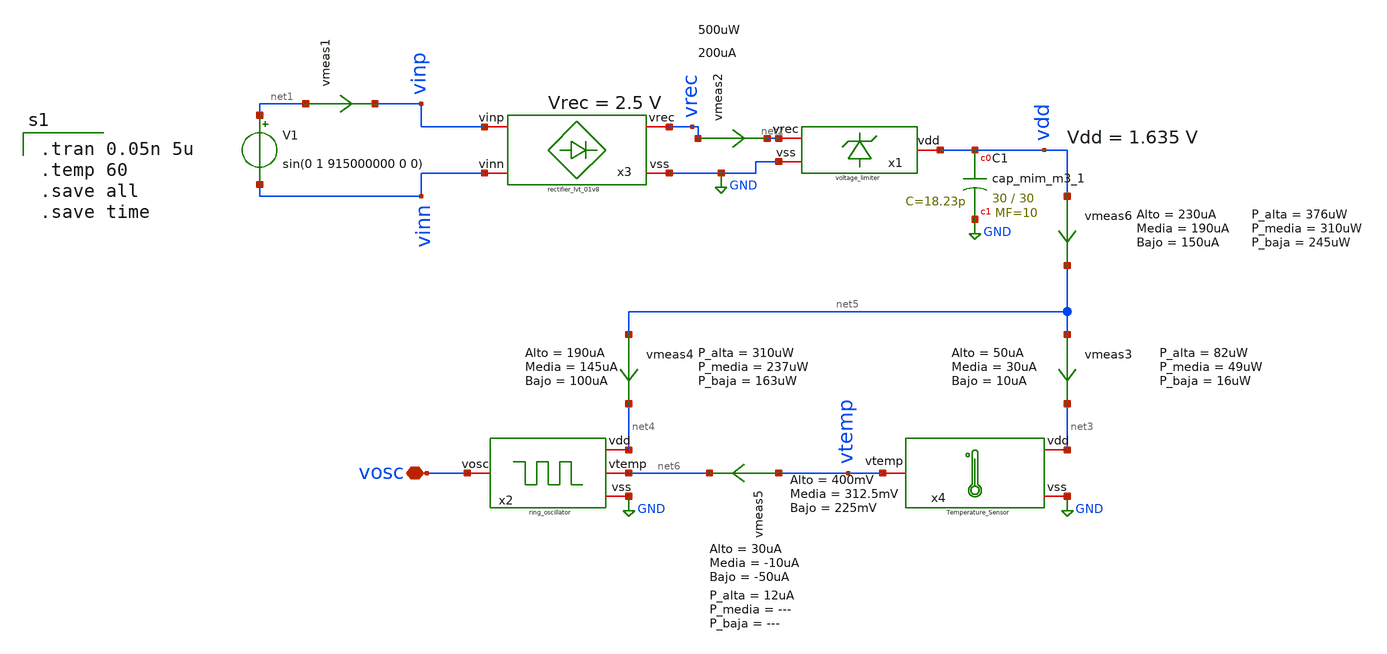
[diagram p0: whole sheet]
** sch_path: XSCHEM/system_on_chip_with_lim.sch
**.subckt system_on_chip_with_lim vosc
*.iopin vosc
V1 net1 vinn sin(0 1 915000000 0 0)
vmeas2 vrec net2 0
.save i(vmeas2)
vmeas1 net1 vinp 0
.save i(vmeas1)
XC1 vdd GND sky130_fd_pr__cap_mim_m3_1 W=30 L=30 MF=10 m=10
x2 net4 vosc GND net6 ring_oscillator
x3 vinp vrec vinn GND rectifier_lvt_01v8
x4 net3 vtemp GND Temperature_Sensor
vmeas3 net5 net3 0
.save i(vmeas3)
vmeas4 net5 net4 0
.save i(vmeas4)
vmeas5 vtemp net6 0
.save i(vmeas5)
x1 net2 vdd GND voltage_limiter
vmeas6 vdd net5 0
.save i(vmeas6)
**** begin user architecture code

.tran 0.05n 5u
.temp 60
.save all
.save time


** opencircuitdesign pdks install
.lib $::SKYWATER_MODELS/sky130.lib.spice tt


**** end user architecture code
**.ends

* expanding   symbol:  Documentos/TESIS DE
*+ GRADO/WORK_IN_PROGRESS/My_xschem_prueba/ring_oscillator.sym # of pins=4
** sym_path: XSCHEM/ring_oscillator.sym
** sch_path: XSCHEM/ring_oscillator.sch
.subckt ring_oscillator vdd vosc vss vtemp
*.iopin vtemp
*.iopin vss
*.iopin vdd
*.iopin vosc
XM7 net1 vosc vdd vdd sky130_fd_pr__pfet_01v8_lvt L=2 W=12 nf=1 ad='int((nf+1)/2) * W/nf * 0.29' as='int((nf+2)/2) * W/nf * 0.29'
+ pd='2*int((nf+1)/2) * (W/nf + 0.29)' ps='2*int((nf+2)/2) * (W/nf + 0.29)' nrd='0.29 / W' nrs='0.29 / W'
+ sa=0 sb=0 sd=0 mult=1 m=1
XM8 net1 vosc vss vss sky130_fd_pr__nfet_01v8_lvt L=2 W=4 nf=1 ad='int((nf+1)/2) * W/nf * 0.29' as='int((nf+2)/2) * W/nf * 0.29'
+ pd='2*int((nf+1)/2) * (W/nf + 0.29)' ps='2*int((nf+2)/2) * (W/nf + 0.29)' nrd='0.29 / W' nrs='0.29 / W'
+ sa=0 sb=0 sd=0 mult=1 m=1
XM9 net2 net1 vdd vdd sky130_fd_pr__pfet_01v8_lvt L=2 W=12 nf=1 ad='int((nf+1)/2) * W/nf * 0.29' as='int((nf+2)/2) * W/nf * 0.29'
+ pd='2*int((nf+1)/2) * (W/nf + 0.29)' ps='2*int((nf+2)/2) * (W/nf + 0.29)' nrd='0.29 / W' nrs='0.29 / W'
+ sa=0 sb=0 sd=0 mult=1 m=1
XM10 net2 net1 vss vss sky130_fd_pr__nfet_01v8_lvt L=2 W=4 nf=1 ad='int((nf+1)/2) * W/nf * 0.29' as='int((nf+2)/2) * W/nf * 0.29'
+ pd='2*int((nf+1)/2) * (W/nf + 0.29)' ps='2*int((nf+2)/2) * (W/nf + 0.29)' nrd='0.29 / W' nrs='0.29 / W'
+ sa=0 sb=0 sd=0 mult=1 m=1
XM11 vosc net2 vdd vdd sky130_fd_pr__pfet_01v8_lvt L=2 W=12 nf=1 ad='int((nf+1)/2) * W/nf * 0.29' as='int((nf+2)/2) * W/nf * 0.29'
+ pd='2*int((nf+1)/2) * (W/nf + 0.29)' ps='2*int((nf+2)/2) * (W/nf + 0.29)' nrd='0.29 / W' nrs='0.29 / W'
+ sa=0 sb=0 sd=0 mult=1 m=1
XM12 vosc net2 vss vss sky130_fd_pr__nfet_01v8_lvt L=2 W=4 nf=1 ad='int((nf+1)/2) * W/nf * 0.29' as='int((nf+2)/2) * W/nf * 0.29'
+ pd='2*int((nf+1)/2) * (W/nf + 0.29)' ps='2*int((nf+2)/2) * (W/nf + 0.29)' nrd='0.29 / W' nrs='0.29 / W'
+ sa=0 sb=0 sd=0 mult=1 m=1
XC1 vosc vtemp vss sky130_fd_pr__cap_var_lvt W=5 L=5 VM=1 m=1
XC2 net2 vtemp vss sky130_fd_pr__cap_var_lvt W=5 L=5 VM=1 m=1
XC3 net1 vtemp vss sky130_fd_pr__cap_var_lvt W=5 L=5 VM=1 m=1
.ends


* expanding   symbol:  Documentos/TESIS DE
*+ GRADO/WORK_IN_PROGRESS/My_xschem_prueba/rectifier_lvt_01v8.sym # of pins=4
** sym_path: XSCHEM/rectifier_lvt_01v8.sym
** sch_path: XSCHEM/rectifier_lvt_01v8.sch
.subckt rectifier_lvt_01v8 vinp vrec vinn vss
*.iopin vinp
*.iopin vinn
*.iopin vss
*.iopin vrec
XC11 vinp net3 sky130_fd_pr__cap_mim_m3_1 W=30 L=30 MF=1 m=1
XC12 net2 vinn sky130_fd_pr__cap_mim_m3_1 W=30 L=30 MF=1 m=1
XC13 vinp net6 sky130_fd_pr__cap_mim_m3_1 W=30 L=30 MF=1 m=1
XC14 net5 vinn sky130_fd_pr__cap_mim_m3_1 W=30 L=30 MF=1 m=1
XM25 vinp vinn vss vss sky130_fd_pr__nfet_01v8_lvt L=0.18 W=5 nf=1 ad='int((nf+1)/2) * W/nf * 0.29' as='int((nf+2)/2) * W/nf * 0.29'
+ pd='2*int((nf+1)/2) * (W/nf + 0.29)' ps='2*int((nf+2)/2) * (W/nf + 0.29)' nrd='0.29 / W' nrs='0.29 / W'
+ sa=0 sb=0 sd=0 mult=6 m=6
XM26 vinn vinp vss vss sky130_fd_pr__nfet_01v8_lvt L=0.18 W=5 nf=1 ad='int((nf+1)/2) * W/nf * 0.29' as='int((nf+2)/2) * W/nf * 0.29'
+ pd='2*int((nf+1)/2) * (W/nf + 0.29)' ps='2*int((nf+2)/2) * (W/nf + 0.29)' nrd='0.29 / W' nrs='0.29 / W'
+ sa=0 sb=0 sd=0 mult=6 m=6
XM27 vinp vinn net1 net1 sky130_fd_pr__pfet_01v8_lvt L=0.35 W=10 nf=2 ad='int((nf+1)/2) * W/nf * 0.29'
+ as='int((nf+2)/2) * W/nf * 0.29' pd='2*int((nf+1)/2) * (W/nf + 0.29)' ps='2*int((nf+2)/2) * (W/nf + 0.29)'
+ nrd='0.29 / W' nrs='0.29 / W' sa=0 sb=0 sd=0 mult=3 m=3
XM28 vinn vinp net1 net1 sky130_fd_pr__pfet_01v8_lvt L=0.35 W=10 nf=2 ad='int((nf+1)/2) * W/nf * 0.29'
+ as='int((nf+2)/2) * W/nf * 0.29' pd='2*int((nf+1)/2) * (W/nf + 0.29)' ps='2*int((nf+2)/2) * (W/nf + 0.29)'
+ nrd='0.29 / W' nrs='0.29 / W' sa=0 sb=0 sd=0 mult=3 m=3
XM29 net3 net2 net1 vss sky130_fd_pr__nfet_01v8_lvt L=0.18 W=5 nf=1 ad='int((nf+1)/2) * W/nf * 0.29'
+ as='int((nf+2)/2) * W/nf * 0.29' pd='2*int((nf+1)/2) * (W/nf + 0.29)' ps='2*int((nf+2)/2) * (W/nf + 0.29)'
+ nrd='0.29 / W' nrs='0.29 / W' sa=0 sb=0 sd=0 mult=6 m=6
XM30 net2 net3 net1 vss sky130_fd_pr__nfet_01v8_lvt L=0.18 W=5 nf=1 ad='int((nf+1)/2) * W/nf * 0.29'
+ as='int((nf+2)/2) * W/nf * 0.29' pd='2*int((nf+1)/2) * (W/nf + 0.29)' ps='2*int((nf+2)/2) * (W/nf + 0.29)'
+ nrd='0.29 / W' nrs='0.29 / W' sa=0 sb=0 sd=0 mult=6 m=6
XM31 net3 net2 net4 net4 sky130_fd_pr__pfet_01v8_lvt L=0.35 W=10 nf=2 ad='int((nf+1)/2) * W/nf * 0.29'
+ as='int((nf+2)/2) * W/nf * 0.29' pd='2*int((nf+1)/2) * (W/nf + 0.29)' ps='2*int((nf+2)/2) * (W/nf + 0.29)'
+ nrd='0.29 / W' nrs='0.29 / W' sa=0 sb=0 sd=0 mult=3 m=3
XM32 net2 net3 net4 net4 sky130_fd_pr__pfet_01v8_lvt L=0.35 W=10 nf=2 ad='int((nf+1)/2) * W/nf * 0.29'
+ as='int((nf+2)/2) * W/nf * 0.29' pd='2*int((nf+1)/2) * (W/nf + 0.29)' ps='2*int((nf+2)/2) * (W/nf + 0.29)'
+ nrd='0.29 / W' nrs='0.29 / W' sa=0 sb=0 sd=0 mult=3 m=3
XM33 net6 net5 net4 vss sky130_fd_pr__nfet_01v8_lvt L=0.18 W=5 nf=1 ad='int((nf+1)/2) * W/nf * 0.29'
+ as='int((nf+2)/2) * W/nf * 0.29' pd='2*int((nf+1)/2) * (W/nf + 0.29)' ps='2*int((nf+2)/2) * (W/nf + 0.29)'
+ nrd='0.29 / W' nrs='0.29 / W' sa=0 sb=0 sd=0 mult=6 m=6
XM34 net5 net6 net4 vss sky130_fd_pr__nfet_01v8_lvt L=0.18 W=5 nf=1 ad='int((nf+1)/2) * W/nf * 0.29'
+ as='int((nf+2)/2) * W/nf * 0.29' pd='2*int((nf+1)/2) * (W/nf + 0.29)' ps='2*int((nf+2)/2) * (W/nf + 0.29)'
+ nrd='0.29 / W' nrs='0.29 / W' sa=0 sb=0 sd=0 mult=6 m=6
XM35 net6 net5 net7 net7 sky130_fd_pr__pfet_01v8_lvt L=0.35 W=10 nf=2 ad='int((nf+1)/2) * W/nf * 0.29'
+ as='int((nf+2)/2) * W/nf * 0.29' pd='2*int((nf+1)/2) * (W/nf + 0.29)' ps='2*int((nf+2)/2) * (W/nf + 0.29)'
+ nrd='0.29 / W' nrs='0.29 / W' sa=0 sb=0 sd=0 mult=3 m=3
XM36 net5 net6 net7 net7 sky130_fd_pr__pfet_01v8_lvt L=0.35 W=10 nf=2 ad='int((nf+1)/2) * W/nf * 0.29'
+ as='int((nf+2)/2) * W/nf * 0.29' pd='2*int((nf+1)/2) * (W/nf + 0.29)' ps='2*int((nf+2)/2) * (W/nf + 0.29)'
+ nrd='0.29 / W' nrs='0.29 / W' sa=0 sb=0 sd=0 mult=3 m=3
XC15 vinp net9 sky130_fd_pr__cap_mim_m3_1 W=30 L=30 MF=1 m=1
XC16 net8 vinn sky130_fd_pr__cap_mim_m3_1 W=30 L=30 MF=1 m=1
XM37 net9 net8 net7 vss sky130_fd_pr__nfet_01v8_lvt L=0.18 W=5 nf=1 ad='int((nf+1)/2) * W/nf * 0.29'
+ as='int((nf+2)/2) * W/nf * 0.29' pd='2*int((nf+1)/2) * (W/nf + 0.29)' ps='2*int((nf+2)/2) * (W/nf + 0.29)'
+ nrd='0.29 / W' nrs='0.29 / W' sa=0 sb=0 sd=0 mult=6 m=6
XM38 net8 net9 net7 vss sky130_fd_pr__nfet_01v8_lvt L=0.18 W=5 nf=1 ad='int((nf+1)/2) * W/nf * 0.29'
+ as='int((nf+2)/2) * W/nf * 0.29' pd='2*int((nf+1)/2) * (W/nf + 0.29)' ps='2*int((nf+2)/2) * (W/nf + 0.29)'
+ nrd='0.29 / W' nrs='0.29 / W' sa=0 sb=0 sd=0 mult=6 m=6
XM39 net9 net8 net10 net10 sky130_fd_pr__pfet_01v8_lvt L=0.35 W=10 nf=2 ad='int((nf+1)/2) * W/nf * 0.29'
+ as='int((nf+2)/2) * W/nf * 0.29' pd='2*int((nf+1)/2) * (W/nf + 0.29)' ps='2*int((nf+2)/2) * (W/nf + 0.29)'
+ nrd='0.29 / W' nrs='0.29 / W' sa=0 sb=0 sd=0 mult=3 m=3
XM40 net8 net9 net10 net10 sky130_fd_pr__pfet_01v8_lvt L=0.35 W=10 nf=2 ad='int((nf+1)/2) * W/nf * 0.29'
+ as='int((nf+2)/2) * W/nf * 0.29' pd='2*int((nf+1)/2) * (W/nf + 0.29)' ps='2*int((nf+2)/2) * (W/nf + 0.29)'
+ nrd='0.29 / W' nrs='0.29 / W' sa=0 sb=0 sd=0 mult=3 m=3
XC17 vinp net12 sky130_fd_pr__cap_mim_m3_1 W=30 L=30 MF=1 m=1
XC18 net11 vinn sky130_fd_pr__cap_mim_m3_1 W=30 L=30 MF=1 m=1
XM41 net12 net11 net10 vss sky130_fd_pr__nfet_01v8_lvt L=0.18 W=5 nf=1 ad='int((nf+1)/2) * W/nf * 0.29'
+ as='int((nf+2)/2) * W/nf * 0.29' pd='2*int((nf+1)/2) * (W/nf + 0.29)' ps='2*int((nf+2)/2) * (W/nf + 0.29)'
+ nrd='0.29 / W' nrs='0.29 / W' sa=0 sb=0 sd=0 mult=6 m=6
XM42 net11 net12 net10 vss sky130_fd_pr__nfet_01v8_lvt L=0.18 W=5 nf=1 ad='int((nf+1)/2) * W/nf * 0.29'
+ as='int((nf+2)/2) * W/nf * 0.29' pd='2*int((nf+1)/2) * (W/nf + 0.29)' ps='2*int((nf+2)/2) * (W/nf + 0.29)'
+ nrd='0.29 / W' nrs='0.29 / W' sa=0 sb=0 sd=0 mult=6 m=6
XM43 net12 net11 net13 net13 sky130_fd_pr__pfet_01v8_lvt L=0.35 W=10 nf=2 ad='int((nf+1)/2) * W/nf * 0.29'
+ as='int((nf+2)/2) * W/nf * 0.29' pd='2*int((nf+1)/2) * (W/nf + 0.29)' ps='2*int((nf+2)/2) * (W/nf + 0.29)'
+ nrd='0.29 / W' nrs='0.29 / W' sa=0 sb=0 sd=0 mult=3 m=3
XM44 net11 net12 net13 net13 sky130_fd_pr__pfet_01v8_lvt L=0.35 W=10 nf=2 ad='int((nf+1)/2) * W/nf * 0.29'
+ as='int((nf+2)/2) * W/nf * 0.29' pd='2*int((nf+1)/2) * (W/nf + 0.29)' ps='2*int((nf+2)/2) * (W/nf + 0.29)'
+ nrd='0.29 / W' nrs='0.29 / W' sa=0 sb=0 sd=0 mult=3 m=3
XC19 vrec vss sky130_fd_pr__cap_mim_m3_1 W=30 L=30 MF=2 m=2
XC20 vinp net15 sky130_fd_pr__cap_mim_m3_1 W=30 L=30 MF=1 m=1
XC21 net14 vinn sky130_fd_pr__cap_mim_m3_1 W=30 L=30 MF=1 m=1
XM45 net15 net14 net13 vss sky130_fd_pr__nfet_01v8_lvt L=0.18 W=5 nf=1 ad='int((nf+1)/2) * W/nf * 0.29'
+ as='int((nf+2)/2) * W/nf * 0.29' pd='2*int((nf+1)/2) * (W/nf + 0.29)' ps='2*int((nf+2)/2) * (W/nf + 0.29)'
+ nrd='0.29 / W' nrs='0.29 / W' sa=0 sb=0 sd=0 mult=6 m=6
XM46 net14 net15 net13 vss sky130_fd_pr__nfet_01v8_lvt L=0.18 W=5 nf=1 ad='int((nf+1)/2) * W/nf * 0.29'
+ as='int((nf+2)/2) * W/nf * 0.29' pd='2*int((nf+1)/2) * (W/nf + 0.29)' ps='2*int((nf+2)/2) * (W/nf + 0.29)'
+ nrd='0.29 / W' nrs='0.29 / W' sa=0 sb=0 sd=0 mult=6 m=6
XM47 net15 net14 vrec vrec sky130_fd_pr__pfet_01v8_lvt L=0.35 W=10 nf=2 ad='int((nf+1)/2) * W/nf * 0.29'
+ as='int((nf+2)/2) * W/nf * 0.29' pd='2*int((nf+1)/2) * (W/nf + 0.29)' ps='2*int((nf+2)/2) * (W/nf + 0.29)'
+ nrd='0.29 / W' nrs='0.29 / W' sa=0 sb=0 sd=0 mult=3 m=3
XM48 net14 net15 vrec vrec sky130_fd_pr__pfet_01v8_lvt L=0.35 W=10 nf=2 ad='int((nf+1)/2) * W/nf * 0.29'
+ as='int((nf+2)/2) * W/nf * 0.29' pd='2*int((nf+1)/2) * (W/nf + 0.29)' ps='2*int((nf+2)/2) * (W/nf + 0.29)'
+ nrd='0.29 / W' nrs='0.29 / W' sa=0 sb=0 sd=0 mult=3 m=3
.ends


* expanding   symbol:  Documentos/TESIS DE
*+ GRADO/WORK_IN_PROGRESS/My_xschem_prueba/Temperature_Sensor.sym # of pins=3
** sym_path: XSCHEM/Temperature_Sensor.sym
** sch_path: XSCHEM/Temperature_Sensor.sch
.subckt Temperature_Sensor vdd vtemp vss
*.iopin vdd
*.iopin vss
*.iopin vtemp
XM8 net1 net4 net2 vss sky130_fd_pr__nfet_01v8_lvt L=2 W=1 nf=1 ad='int((nf+1)/2) * W/nf * 0.29' as='int((nf+2)/2) * W/nf * 0.29'
+ pd='2*int((nf+1)/2) * (W/nf + 0.29)' ps='2*int((nf+2)/2) * (W/nf + 0.29)' nrd='0.29 / W' nrs='0.29 / W'
+ sa=0 sb=0 sd=0 mult=4 m=4
XM9 vtemp net3 net2 vss sky130_fd_pr__nfet_01v8_lvt L=0.5 W=1 nf=1 ad='int((nf+1)/2) * W/nf * 0.29' as='int((nf+2)/2) * W/nf * 0.29'
+ pd='2*int((nf+1)/2) * (W/nf + 0.29)' ps='2*int((nf+2)/2) * (W/nf + 0.29)' nrd='0.29 / W' nrs='0.29 / W'
+ sa=0 sb=0 sd=0 mult=4 m=4
XM10 net2 net5 vss vss sky130_fd_pr__nfet_01v8 L=2 W=5 nf=1 ad='int((nf+1)/2) * W/nf * 0.29' as='int((nf+2)/2) * W/nf * 0.29'
+ pd='2*int((nf+1)/2) * (W/nf + 0.29)' ps='2*int((nf+2)/2) * (W/nf + 0.29)' nrd='0.29 / W' nrs='0.29 / W'
+ sa=0 sb=0 sd=0 mult=4 m=4
XM11 net1 net1 vdd vdd sky130_fd_pr__pfet_01v8_lvt L=2 W=5 nf=1 ad='int((nf+1)/2) * W/nf * 0.29' as='int((nf+2)/2) * W/nf * 0.29'
+ pd='2*int((nf+1)/2) * (W/nf + 0.29)' ps='2*int((nf+2)/2) * (W/nf + 0.29)' nrd='0.29 / W' nrs='0.29 / W'
+ sa=0 sb=0 sd=0 mult=4 m=4
XM12 vtemp net1 vdd vdd sky130_fd_pr__pfet_01v8_lvt L=2 W=5 nf=1 ad='int((nf+1)/2) * W/nf * 0.29' as='int((nf+2)/2) * W/nf * 0.29'
+ pd='2*int((nf+1)/2) * (W/nf + 0.29)' ps='2*int((nf+2)/2) * (W/nf + 0.29)' nrd='0.29 / W' nrs='0.29 / W'
+ sa=0 sb=0 sd=0 mult=4 m=4
XM13 net6 net6 net4 vss sky130_fd_pr__nfet_01v8_lvt L=2 W=4 nf=1 ad='int((nf+1)/2) * W/nf * 0.29' as='int((nf+2)/2) * W/nf * 0.29'
+ pd='2*int((nf+1)/2) * (W/nf + 0.29)' ps='2*int((nf+2)/2) * (W/nf + 0.29)' nrd='0.29 / W' nrs='0.29 / W'
+ sa=0 sb=0 sd=0 mult=1 m=1
XQ3 vss vss net4 sky130_fd_pr__pnp_05v5_W3p40L3p40 m=1
XM14 vdd net6 net3 vss sky130_fd_pr__nfet_01v8_lvt L=2 W=4 nf=1 ad='int((nf+1)/2) * W/nf * 0.29' as='int((nf+2)/2) * W/nf * 0.29'
+ pd='2*int((nf+1)/2) * (W/nf + 0.29)' ps='2*int((nf+2)/2) * (W/nf + 0.29)' nrd='0.29 / W' nrs='0.29 / W'
+ sa=0 sb=0 sd=0 mult=10 m=10
XQ4 vss vss net3 sky130_fd_pr__pnp_05v5_W3p40L3p40 m=1
XM7 net6 net5 vdd vdd sky130_fd_pr__pfet_01v8_lvt L=2 W=2 nf=1 ad='int((nf+1)/2) * W/nf * 0.29' as='int((nf+2)/2) * W/nf * 0.29'
+ pd='2*int((nf+1)/2) * (W/nf + 0.29)' ps='2*int((nf+2)/2) * (W/nf + 0.29)' nrd='0.29 / W' nrs='0.29 / W'
+ sa=0 sb=0 sd=0 mult=1 m=1
XM20 net7 net7 vdd vdd sky130_fd_pr__pfet_01v8_lvt L=2 W=2 nf=1 ad='int((nf+1)/2) * W/nf * 0.29' as='int((nf+2)/2) * W/nf * 0.29'
+ pd='2*int((nf+1)/2) * (W/nf + 0.29)' ps='2*int((nf+2)/2) * (W/nf + 0.29)' nrd='0.29 / W' nrs='0.29 / W'
+ sa=0 sb=0 sd=0 mult=1 m=1
XM21 net5 net5 vss vss sky130_fd_pr__nfet_01v8_lvt L=2 W=0.5 nf=1 ad='int((nf+1)/2) * W/nf * 0.29' as='int((nf+2)/2) * W/nf * 0.29'
+ pd='2*int((nf+1)/2) * (W/nf + 0.29)' ps='2*int((nf+2)/2) * (W/nf + 0.29)' nrd='0.29 / W' nrs='0.29 / W'
+ sa=0 sb=0 sd=0 mult=1 m=1
XM22 net8 net7 vdd vdd sky130_fd_pr__pfet_01v8_lvt L=2 W=2 nf=1 ad='int((nf+1)/2) * W/nf * 0.29' as='int((nf+2)/2) * W/nf * 0.29'
+ pd='2*int((nf+1)/2) * (W/nf + 0.29)' ps='2*int((nf+2)/2) * (W/nf + 0.29)' nrd='0.29 / W' nrs='0.29 / W'
+ sa=0 sb=0 sd=0 mult=1 m=1
XM23 net9 net5 net8 vdd sky130_fd_pr__pfet_01v8_lvt L=2 W=2 nf=1 ad='int((nf+1)/2) * W/nf * 0.29' as='int((nf+2)/2) * W/nf * 0.29'
+ pd='2*int((nf+1)/2) * (W/nf + 0.29)' ps='2*int((nf+2)/2) * (W/nf + 0.29)' nrd='0.29 / W' nrs='0.29 / W'
+ sa=0 sb=0 sd=0 mult=1 m=1
XM24 net5 net5 net7 vdd sky130_fd_pr__pfet_01v8_lvt L=2 W=2 nf=1 ad='int((nf+1)/2) * W/nf * 0.29' as='int((nf+2)/2) * W/nf * 0.29'
+ pd='2*int((nf+1)/2) * (W/nf + 0.29)' ps='2*int((nf+2)/2) * (W/nf + 0.29)' nrd='0.29 / W' nrs='0.29 / W'
+ sa=0 sb=0 sd=0 mult=1 m=1
XM25 net9 net9 vss vss sky130_fd_pr__nfet_01v8_lvt L=2 W=0.5 nf=1 ad='int((nf+1)/2) * W/nf * 0.29' as='int((nf+2)/2) * W/nf * 0.29'
+ pd='2*int((nf+1)/2) * (W/nf + 0.29)' ps='2*int((nf+2)/2) * (W/nf + 0.29)' nrd='0.29 / W' nrs='0.29 / W'
+ sa=0 sb=0 sd=0 mult=1 m=1
.ends


* expanding   symbol:  Documentos/TESIS DE
*+ GRADO/WORK_IN_PROGRESS/My_xschem_prueba/voltage_limiter.sym # of pins=3
** sym_path: XSCHEM/voltage_limiter.sym
** sch_path: XSCHEM/voltage_limiter.sch
.subckt voltage_limiter vrec vdd vss
*.iopin vss
*.iopin vrec
*.iopin vdd
XM4 net1 net4 vss vss sky130_fd_pr__nfet_01v8_lvt L=0.7 W=2 nf=1 ad='int((nf+1)/2) * W/nf * 0.29' as='int((nf+2)/2) * W/nf * 0.29'
+ pd='2*int((nf+1)/2) * (W/nf + 0.29)' ps='2*int((nf+2)/2) * (W/nf + 0.29)' nrd='0.29 / W' nrs='0.29 / W'
+ sa=0 sb=0 sd=0 mult=1 m=1
XM5 vss net1 vdd vdd sky130_fd_pr__pfet_01v8_lvt L=0.35 W=16 nf=4 ad='int((nf+1)/2) * W/nf * 0.29' as='int((nf+2)/2) * W/nf * 0.29'
+ pd='2*int((nf+1)/2) * (W/nf + 0.29)' ps='2*int((nf+2)/2) * (W/nf + 0.29)' nrd='0.29 / W' nrs='0.29 / W'
+ sa=0 sb=0 sd=0 mult=1 m=1
XM1 net2 net2 vdd vdd sky130_fd_pr__pfet_01v8_lvt L=0.35 W=4 nf=1 ad='int((nf+1)/2) * W/nf * 0.29' as='int((nf+2)/2) * W/nf * 0.29'
+ pd='2*int((nf+1)/2) * (W/nf + 0.29)' ps='2*int((nf+2)/2) * (W/nf + 0.29)' nrd='0.29 / W' nrs='0.29 / W'
+ sa=0 sb=0 sd=0 mult=2 m=2
XM2 net3 net3 net2 vdd sky130_fd_pr__pfet_01v8_lvt L=0.35 W=4 nf=1 ad='int((nf+1)/2) * W/nf * 0.29' as='int((nf+2)/2) * W/nf * 0.29'
+ pd='2*int((nf+1)/2) * (W/nf + 0.29)' ps='2*int((nf+2)/2) * (W/nf + 0.29)' nrd='0.29 / W' nrs='0.29 / W'
+ sa=0 sb=0 sd=0 mult=2 m=2
XM3 net4 net4 net3 vdd sky130_fd_pr__pfet_01v8_lvt L=0.35 W=4 nf=1 ad='int((nf+1)/2) * W/nf * 0.29' as='int((nf+2)/2) * W/nf * 0.29'
+ pd='2*int((nf+1)/2) * (W/nf + 0.29)' ps='2*int((nf+2)/2) * (W/nf + 0.29)' nrd='0.29 / W' nrs='0.29 / W'
+ sa=0 sb=0 sd=0 mult=2 m=2
XR2 net1 vdd vss sky130_fd_pr__res_xhigh_po W=1 L=60 mult=1 m=1
XR4 vss net4 vss sky130_fd_pr__res_xhigh_po W=1 L=40 mult=1 m=1
R1 vdd vrec sky130_fd_pr__res_generic_l1 W=1 L=18 m=1
.ends

.GLOBAL GND
.end
